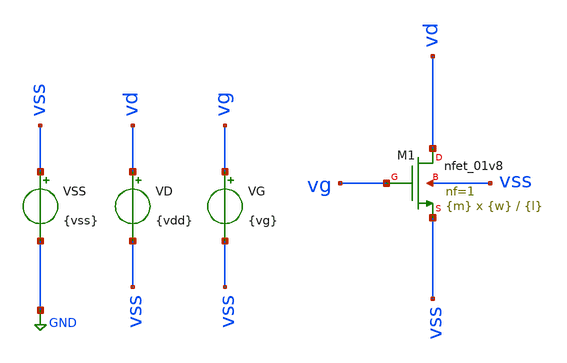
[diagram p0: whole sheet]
** sch_path: sch/nmos/nmos.sch
**.subckt nmos
XM1 vd vg vss vss sky130_fd_pr__nfet_01v8 L={l} W={w} nf=1 ad='int((nf+1)/2) * W/nf * 0.29' as='int((nf+2)/2) * W/nf * 0.29'
+ pd='2*int((nf+1)/2) * (W/nf + 0.29)' ps='2*int((nf+2)/2) * (W/nf + 0.29)' nrd='0.29 / W' nrs='0.29 / W'
+ sa=0 sb=0 sd=0 mult={m} m={m}
VG vg vss {vg}
VD vd vss {vdd}
VSS vss GND {vss}
**.ends
.GLOBAL GND
.end
